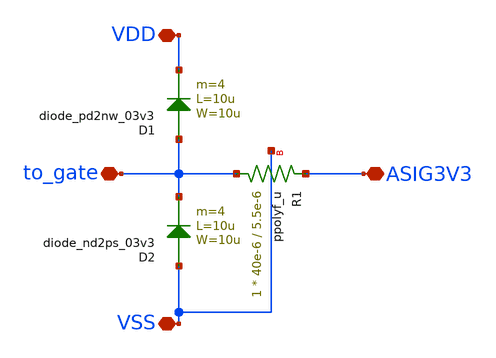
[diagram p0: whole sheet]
** sch_path: designs/libs/secondary_esd/io_secondary_3p3.sch
**.subckt io_secondary_3p3 VSS VDD to_gate ASIG3V3
*.iopin VSS
*.iopin VDD
*.iopin to_gate
*.iopin ASIG3V3
XR1 to_gate ASIG3V3 VSS ppolyf_u r_width=40e-6 r_length=5.5e-6 m=1
D2 VSS to_gate diode_nd2ps_03v3 area='10u * 10u ' pj='2*10u + 2*10u ' m=4
D1 to_gate VDD diode_pd2nw_03v3 area='10u * 10u ' pj='2*10u + 2*10u ' m=4
**.ends
.end
